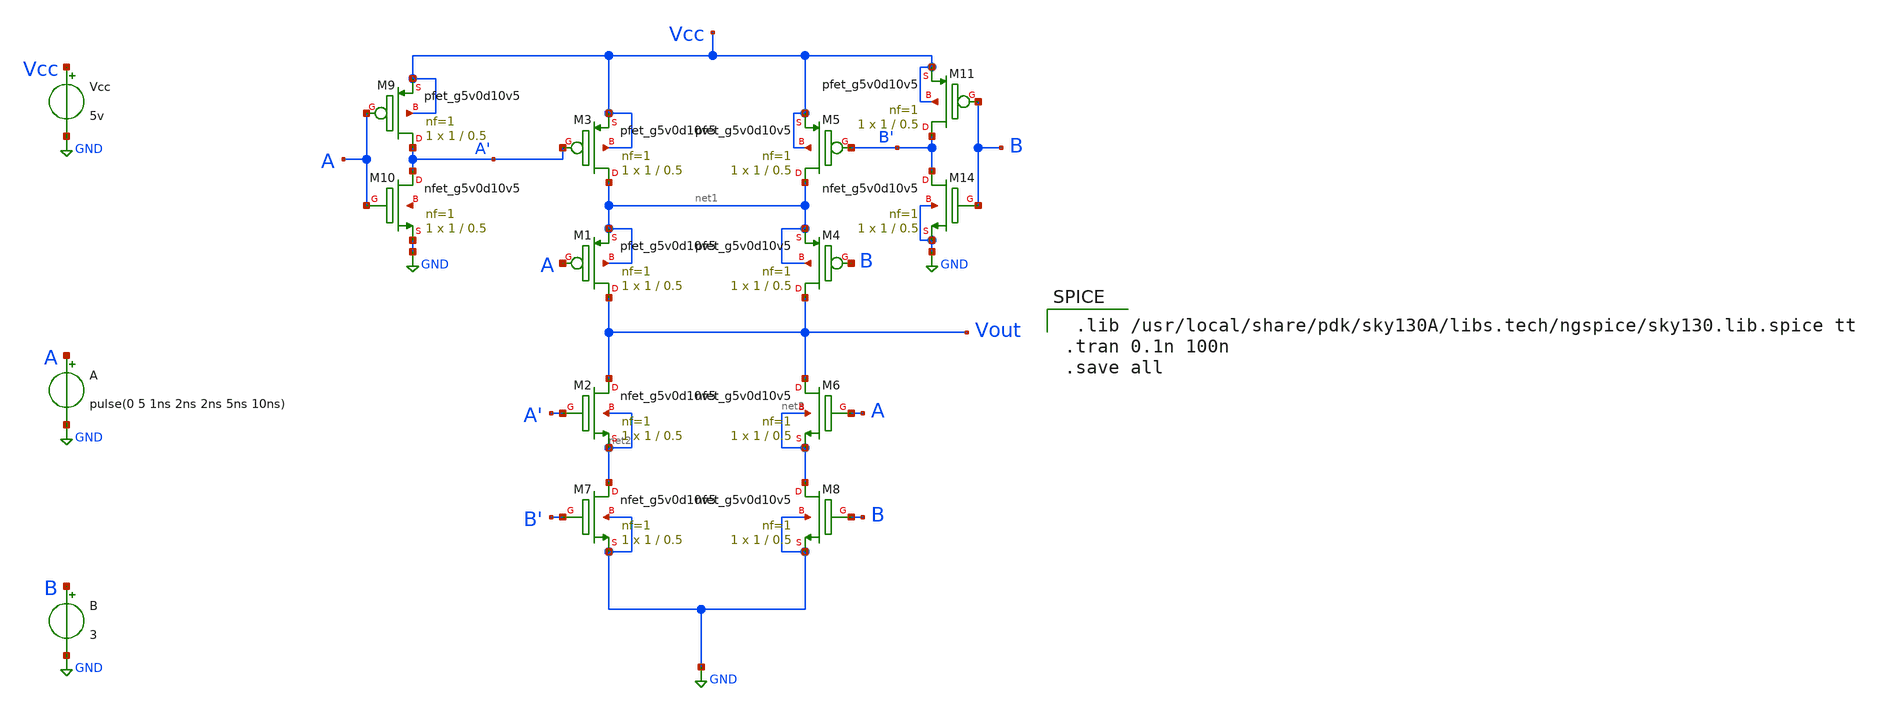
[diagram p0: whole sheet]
** sch_path: Simulation/2ipXOR.sch
**.subckt 2ipXOR
XM1 Vout A net1 net1 sky130_fd_pr__pfet_g5v0d10v5 L=0.5 W=1 nf=1 ad='int((nf+1)/2) * W/nf * 0.29' as='int((nf+2)/2) * W/nf * 0.29'
+ pd='2*int((nf+1)/2) * (W/nf + 0.29)' ps='2*int((nf+2)/2) * (W/nf + 0.29)' nrd='0.29 / W' nrs='0.29 / W'
+ sa=0 sb=0 sd=0 mult=1 m=1
XM2 Vout A' net2 net2 sky130_fd_pr__nfet_g5v0d10v5 L=0.5 W=1 nf=1 ad='int((nf+1)/2) * W/nf * 0.29' as='int((nf+2)/2)
+ * W/nf * 0.29' pd='2*int((nf+1)/2) * (W/nf + 0.29)' ps='2*int((nf+2)/2) * (W/nf + 0.29)' nrd='0.29 /
+ W' nrs='0.29 / W' sa=0 sb=0 sd=0 mult=1 m=1
XM4 Vout B net1 net1 sky130_fd_pr__pfet_g5v0d10v5 L=0.5 W=1 nf=1 ad='int((nf+1)/2) * W/nf * 0.29' as='int((nf+2)/2)
+ * W/nf * 0.29' pd='2*int((nf+1)/2) * (W/nf + 0.29)' ps='2*int((nf+2)/2) * (W/nf + 0.29)' nrd='0.29 /
+ W' nrs='0.29 / W' sa=0 sb=0 sd=0 mult=1 m=1
XM6 Vout A net3 net3 sky130_fd_pr__nfet_g5v0d10v5 L=0.5 W=1 nf=1 ad='int((nf+1)/2) * W/nf * 0.29' as='int((nf+2)/2)
+ * W/nf * 0.29' pd='2*int((nf+1)/2) * (W/nf + 0.29)' ps='2*int((nf+2)/2) * (W/nf + 0.29)' nrd='0.29 /
+ W' nrs='0.29 / W' sa=0 sb=0 sd=0 mult=1 m=1
XM3 net1 A' Vcc Vcc sky130_fd_pr__pfet_g5v0d10v5 L=0.5 W=1 nf=1 ad='int((nf+1)/2) * W/nf * 0.29' as='int((nf+2)/2) * W/nf * 0.29'
+ pd='2*int((nf+1)/2) * (W/nf + 0.29)' ps='2*int((nf+2)/2) * (W/nf + 0.29)' nrd='0.29 / W' nrs='0.29 / W'
+ sa=0 sb=0 sd=0 mult=1 m=1
XM5 net1 B' Vcc Vcc sky130_fd_pr__pfet_g5v0d10v5 L=0.5 W=1 nf=1 ad='int((nf+1)/2) * W/nf * 0.29' as='int((nf+2)/2)
+ * W/nf * 0.29' pd='2*int((nf+1)/2) * (W/nf + 0.29)' ps='2*int((nf+2)/2) * (W/nf + 0.29)' nrd='0.29 /
+ W' nrs='0.29 / W' sa=0 sb=0 sd=0 mult=1 m=1
XM7 net2 B' GND GND sky130_fd_pr__nfet_g5v0d10v5 L=0.5 W=1 nf=1 ad='int((nf+1)/2) * W/nf * 0.29' as='int((nf+2)/2) * W/nf * 0.29'
+ pd='2*int((nf+1)/2) * (W/nf + 0.29)' ps='2*int((nf+2)/2) * (W/nf + 0.29)' nrd='0.29 / W' nrs='0.29 / W'
+ sa=0 sb=0 sd=0 mult=1 m=1
XM8 net3 B GND GND sky130_fd_pr__nfet_g5v0d10v5 L=0.5 W=1 nf=1 ad='int((nf+1)/2) * W/nf * 0.29' as='int((nf+2)/2) * W/nf * 0.29'
+ pd='2*int((nf+1)/2) * (W/nf + 0.29)' ps='2*int((nf+2)/2) * (W/nf + 0.29)' nrd='0.29 / W' nrs='0.29 / W'
+ sa=0 sb=0 sd=0 mult=1 m=1
Vcc Vcc GND 5v
A A GND pulse(0 5 1ns 2ns 2ns 5ns 10ns)
XM9 A' A Vcc Vcc sky130_fd_pr__pfet_g5v0d10v5 L=0.5 W=1 nf=1 ad='int((nf+1)/2) * W/nf * 0.29' as='int((nf+2)/2)
+ * W/nf * 0.29' pd='2*int((nf+1)/2) * (W/nf + 0.29)' ps='2*int((nf+2)/2) * (W/nf + 0.29)' nrd='0.29 /
+ W' nrs='0.29 / W' sa=0 sb=0 sd=0 mult=1 m=1
XM10 A' A GND net4 sky130_fd_pr__nfet_g5v0d10v5 L=0.5 W=1 nf=1 ad='int((nf+1)/2) * W/nf * 0.29' as='int((nf+2)/2) * W/nf * 0.29'
+ pd='2*int((nf+1)/2) * (W/nf + 0.29)' ps='2*int((nf+2)/2) * (W/nf + 0.29)' nrd='0.29 / W' nrs='0.29 / W'
+ sa=0 sb=0 sd=0 mult=1 m=1
XM11 B' B Vcc Vcc sky130_fd_pr__pfet_g5v0d10v5 L=0.5 W=1 nf=1 ad='int((nf+1)/2) * W/nf * 0.29' as='int((nf+2)/2)
+ * W/nf * 0.29' pd='2*int((nf+1)/2) * (W/nf + 0.29)' ps='2*int((nf+2)/2) * (W/nf + 0.29)' nrd='0.29 /
+ W' nrs='0.29 / W' sa=0 sb=0 sd=0 mult=1 m=1
XM14 B' B GND GND sky130_fd_pr__nfet_g5v0d10v5 L=0.5 W=1 nf=1 ad='int((nf+1)/2) * W/nf * 0.29' as='int((nf+2)/2) * W/nf * 0.29'
+ pd='2*int((nf+1)/2) * (W/nf + 0.29)' ps='2*int((nf+2)/2) * (W/nf + 0.29)' nrd='0.29 / W' nrs='0.29 / W'
+ sa=0 sb=0 sd=0 mult=1 m=1
B B GND 3
**** begin user architecture code

 .lib /usr/local/share/pdk/sky130A/libs.tech/ngspice/sky130.lib.spice tt
.tran 0.1n 100n
.save all

**** end user architecture code
**.ends
.GLOBAL GND
.end
